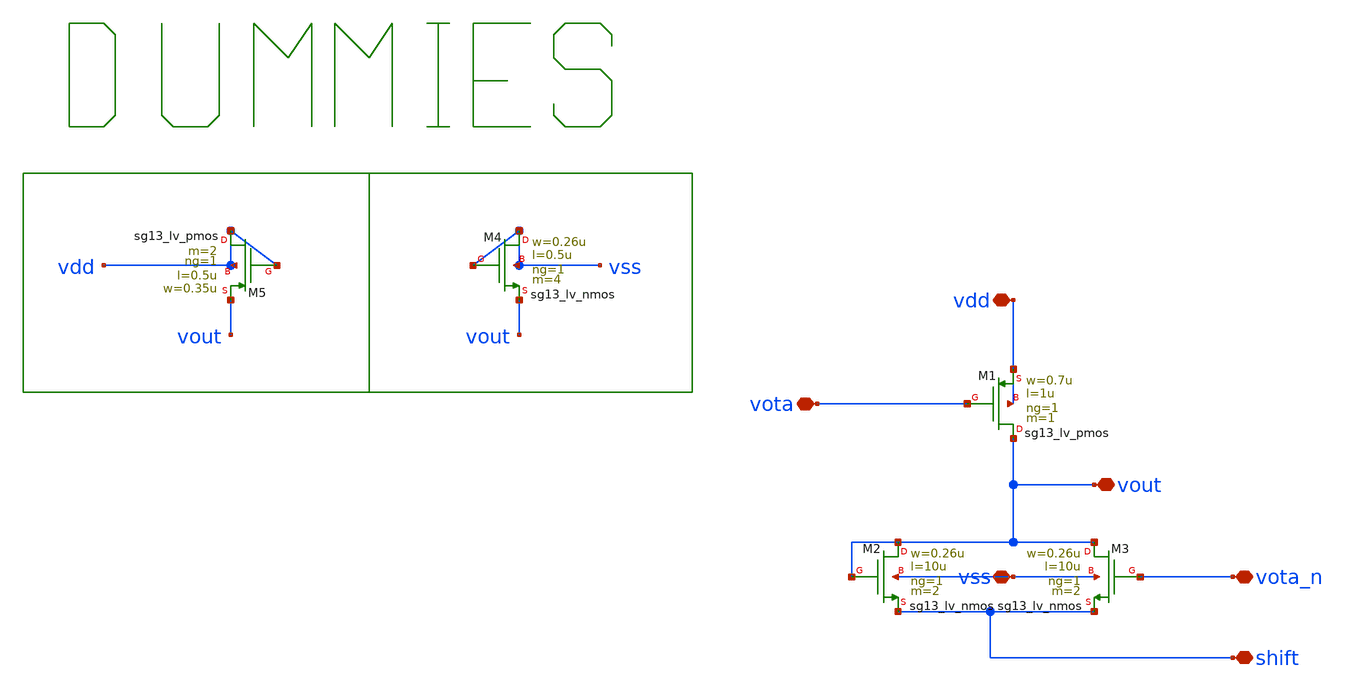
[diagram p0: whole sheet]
** sch_path: schematic/xschem/decision_circuit/decision_circuit.sch
**.subckt decision_circuit vota shift vota_n vdd vss vout
*.iopin vota
*.iopin shift
*.iopin vota_n
*.iopin vdd
*.iopin vss
*.iopin vout
XM1 vout vota vdd vdd sg13_lv_pmos w=0.7u l=1u ng=1 m=1 mm_ok=1
XM2 vout vout shift vss sg13_lv_nmos w=0.26u l=10u ng=1 m=2 mm_ok=1
XM3 vout vota_n shift vss sg13_lv_nmos w=0.26u l=10u ng=1 m=2 mm_ok=1
XM4 vss vss vout vss sg13_lv_nmos w=0.26u l=0.5u ng=1 m=4 mm_ok=1
XM5 vdd vdd vout vdd sg13_lv_pmos w=0.35u l=0.5u ng=1 m=2 mm_ok=1
**.ends
.end
